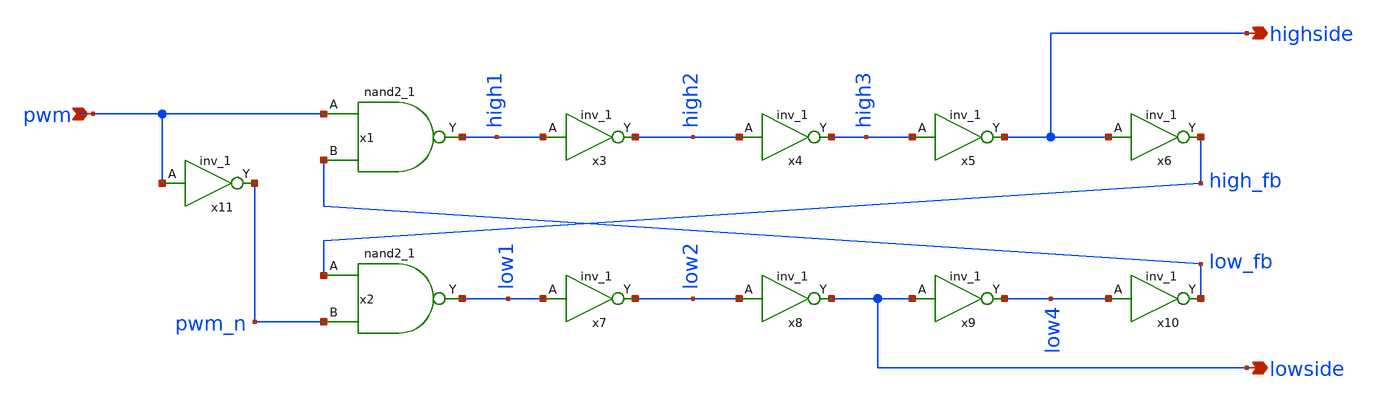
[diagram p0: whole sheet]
** sch_path: Ene_Thompson/deadtime.sch
**.subckt deadtime pwm highside lowside
*.ipin pwm
*.opin highside
*.opin lowside
x1 pwm low_fb VGND VNB VPB VPWR high1 sky130_fd_sc_hd__nand2_1
x2 high_fb pwm_n VGND VNB VPB VPWR low1 sky130_fd_sc_hd__nand2_1
x3 high1 VGND VNB VPB VPWR high2 sky130_fd_sc_hd__inv_1
x4 high2 VGND VNB VPB VPWR high3 sky130_fd_sc_hd__inv_1
x5 high3 VGND VNB VPB VPWR highside sky130_fd_sc_hd__inv_1
x6 highside VGND VNB VPB VPWR high_fb sky130_fd_sc_hd__inv_1
x7 low1 VGND VNB VPB VPWR low2 sky130_fd_sc_hd__inv_1
x8 low2 VGND VNB VPB VPWR lowside sky130_fd_sc_hd__inv_1
x9 lowside VGND VNB VPB VPWR low4 sky130_fd_sc_hd__inv_1
x10 low4 VGND VNB VPB VPWR low_fb sky130_fd_sc_hd__inv_1
x11 pwm VGND VNB VPB VPWR pwm_n sky130_fd_sc_hd__inv_1
**** begin user architecture code

VVPWR VPWR GND 3.6
VVPB VPB GND 3.6
VVGND VGND GND 0
VVNB VNB GND 0

**** end user architecture code
**.ends
.end
